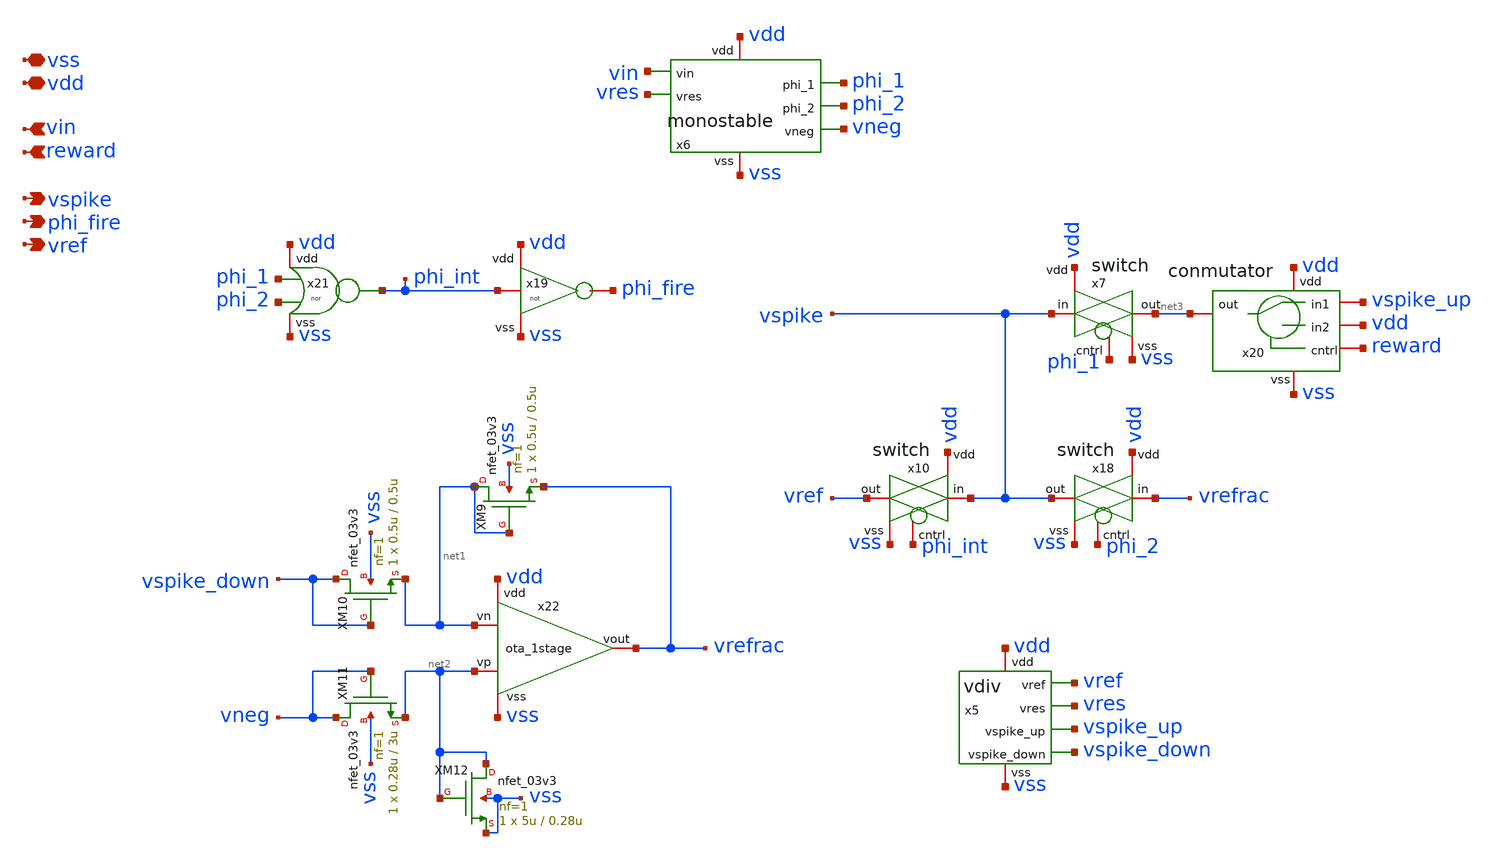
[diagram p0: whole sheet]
** sch_path: designs/libs/core_LIF_comp/core_phaseUpulse/phaseUpulse.sch
**.subckt phaseUpulse vin vdd vss vspike phi_fire vref reward
*.ipin vin
*.iopin vdd
*.iopin vss
*.opin vspike
*.opin phi_fire
*.opin vref
*.ipin reward
x19 vdd phi_int phi_fire vss not
x21 vdd vss phi_1 phi_2 phi_int nor
x22 vdd vrefrac net2 net1 vss ota_1stage
XM9 net1 net1 vrefrac vss nfet_03v3 L=0.5u W=0.5u nf=1 ad='int((nf+1)/2) * W/nf * 0.18u' as='int((nf+2)/2) * W/nf * 0.18u'
+ pd='2*int((nf+1)/2) * (W/nf + 0.18u)' ps='2*int((nf+2)/2) * (W/nf + 0.18u)' nrd='0.18u / W' nrs='0.18u / W'
+ sa=0 sb=0 sd=0 m=1
XM10 vspike_down vspike_down net1 vss nfet_03v3 L=0.5u W=0.5u nf=1 ad='int((nf+1)/2) * W/nf * 0.18u'
+ as='int((nf+2)/2) * W/nf * 0.18u' pd='2*int((nf+1)/2) * (W/nf + 0.18u)' ps='2*int((nf+2)/2) * (W/nf + 0.18u)'
+ nrd='0.18u / W' nrs='0.18u / W' sa=0 sb=0 sd=0 m=1
XM11 vneg vneg net2 vss nfet_03v3 L=3u W=0.28u nf=1 ad='int((nf+1)/2) * W/nf * 0.18u' as='int((nf+2)/2) * W/nf * 0.18u'
+ pd='2*int((nf+1)/2) * (W/nf + 0.18u)' ps='2*int((nf+2)/2) * (W/nf + 0.18u)' nrd='0.18u / W' nrs='0.18u / W'
+ sa=0 sb=0 sd=0 m=1
XM12 net2 net2 vss vss nfet_03v3 L=0.28u W=5u nf=1 ad='int((nf+1)/2) * W/nf * 0.18u' as='int((nf+2)/2) * W/nf * 0.18u'
+ pd='2*int((nf+1)/2) * (W/nf + 0.18u)' ps='2*int((nf+2)/2) * (W/nf + 0.18u)' nrd='0.18u / W' nrs='0.18u / W'
+ sa=0 sb=0 sd=0 m=1
x7 vdd vspike net3 phi_1 vss switch
x10 vdd vspike vref phi_int vss switch
x18 vdd vrefrac vspike phi_2 vss switch
x20 reward vdd vdd net3 vspike_up vss conmutator
x5 vss vdd vref vspike_up vspike_down vres vdiv
x6 vss vdd vin vres phi_1 phi_2 vneg monostable
**.ends
.end
